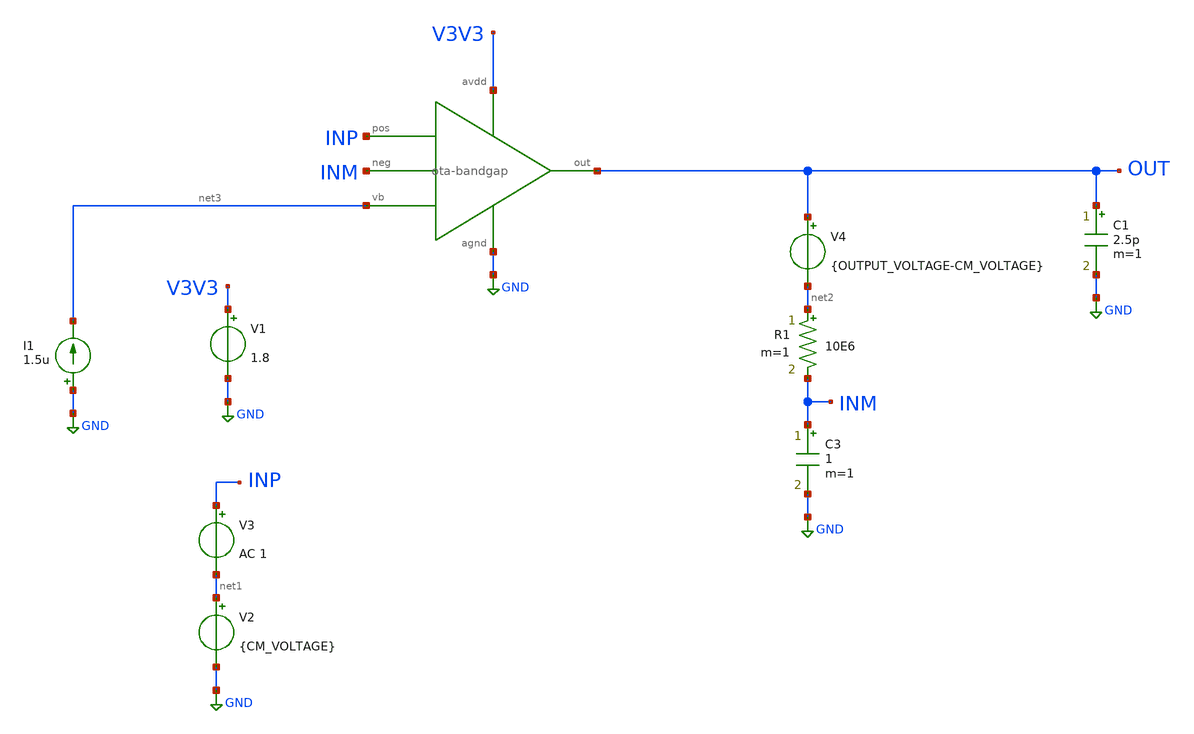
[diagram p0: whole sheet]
** sch_path: LDO/xschem/ota-bandgap/test/ota-bandgap-test.sch
**.subckt ota-bandgap-test
V1 V3V3 GND 1.8
V2 net1 GND {CM_VOLTAGE}
V3 INP net1 AC 1
R1 net2 INM 10E6 m=1
V4 OUT net2 {OUTPUT_VOLTAGE-CM_VOLTAGE}
C3 INM GND 1 m=1
I1 GND net3 1.5u
X1 OUT GND V3V3 INP INM net3 ota-bandgap
C1 OUT GND 2.5p m=1
**** begin user architecture code


.include $env(PDK_ROOT)/$env(PDK)/libs.tech/ngspice/design.ngspice
.lib $env(PDK_ROOT)/$env(PDK)/libs.tech/ngspice/sm141064.ngspice typical
.lib $env(PDK_ROOT)/$env(PDK)/libs.tech/ngspice/sm141064.ngspice mimcap_statistical
.lib $env(PDK_ROOT)/$env(PDK)/libs.tech/ngspice/sm141064.ngspice cap_mim

.options savecurrents

*.lib /foss/pdks/sky130A/libs.tech/ngspice/sky130.lib.spice tt
.param CM_VOLTAGE = 0.9
.param OUTPUT_VOLTAGE = 1
.control
save all
ac dec 200 10 1000Meg
settype decibel out
plot vdb(out)
wrdata /foss/designs/LDO_Design/data/data_OTAvoutdb.dat vdb(out)
let phase_val = 180/PI*cph(out)
let phase_margin_val = 180 + 180/PI*cph(out)
settype phase phase_val
plot phase_val
wrdata /foss/designs/LDO_Design/data/data_OTAphase_val.dat phase_val
meas ac phase_margin find phase_margin_val when vdb(out)=0
meas ac crossover_freq WHEN vdb(out)=0
op

*wrdata /foss/designs/IPD413_2023_HW1_git/data_nmos_gmvgs_VDSp9.dat gmn



*let id1  = @m.x1.xm3.m0[gm]
*let id2  = @m.x1.xm2.msky130_fd_pr__nfet_01v8_lvt[id]
*let id3  = @m.x1.xm3.msky130_fd_pr__pfet_01v8_lvt[id]
*let id4  = @m.x1.xm4.msky130_fd_pr__pfet_01v8_lvt[id]
*let id5  = @m.x1.xm5.msky130_fd_pr__pfet_01v8_lvt[id]
*let id6  = @m.x1.xm6.msky130_fd_pr__nfet_01v8_lvt[id]
*let id7  = @m.x1.xm7.msky130_fd_pr__nfet_01v8_lvt[id]
*let id8  = @m.x1.xm8.msky130_fd_pr__nfet_01v8_lvt[id]

let gm1  = @m.x1.xm1.m0[gm]
*let gm2  = @m.x1.xm2.msky130_fd_pr__nfet_01v8_lvt[gm]
*let gm3  = @m.x1.xm3.msky130_fd_pr__pfet_01v8_lvt[gm]
*let gm4  = @m.x1.xm4.msky130_fd_pr__pfet_01v8_lvt[gm]
let gm5  = @m.x1.xm5.m0[gm]
*let gm6  = @m.x1.xm6.msky130_fd_pr__nfet_01v8_lvt[gm]
*let gm7  = @m.x1.xm7.msky130_fd_pr__nfet_01v8_lvt[gm]
*let gm8  = @m.x1.xm8.msky130_fd_pr__nfet_01v8_lvt[gm]

let gds2 = @m.x1.xm2.m0[gds]
let gds4 = @m.x1.xm4.m0[gds]
let gds5 = @m.x1.xm5.m0[gds]
let gds6 = @m.x1.xm6.m0[gds]


*let vgs1  = @m.x1.xm1.msky130_fd_pr__nfet_01v8_lvt[vgs]
*let vth1  = @m.x1.xm1.msky130_fd_pr__nfet_01v8_lvt[vth]
*let vov1 = vgs1 - vth1
*let vds1  = @m.x1.xm1.msky130_fd_pr__nfet_01v8_lvt[vds]
*let vdsat1  = @m.x1.xm1.msky130_fd_pr__nfet_01v8_lvt[vdsat]

let cgs5  = @m.x1.xm5.m0[cgg]

*@m.xm1.m0[id]
print v(inp)
print v(inm)
print v(out)
let v_offset = v(inp)-v(inm)
print v_offset

print cgs5
*print id1
*print id2
*print id5
*print gm1
*print gm2
*print gm5
*print id7
*print id8
print gm5
print gm1
print gm1/(gds2+gds4)
print gm5/(gds5+gds6)

*print v(vgs1)
*print v(vth1)
*print v(vov1)
*print v(vds1)
*print v(vdsat1)

.endc

**** end user architecture code
**.ends
.GLOBAL GND
.end
